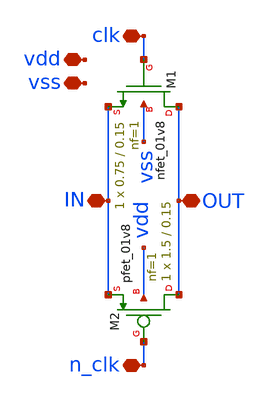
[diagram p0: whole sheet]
** sch_path: sch/TG.sch
**.subckt TG OUT IN clk n_clk vdd vss
*.iopin OUT
*.iopin IN
*.iopin clk
*.iopin n_clk
*.iopin vdd
*.iopin vss
XM1 OUT clk IN vss sky130_fd_pr__nfet_01v8 L=0.15 W=0.75 nf=1 ad='int((nf+1)/2) * W/nf * 0.29' as='int((nf+2)/2) * W/nf * 0.29'
+ pd='2*int((nf+1)/2) * (W/nf + 0.29)' ps='2*int((nf+2)/2) * (W/nf + 0.29)' nrd='0.29 / W' nrs='0.29 / W'
+ sa=0 sb=0 sd=0 mult=1 m=1
XM2 OUT n_clk IN vdd sky130_fd_pr__pfet_01v8 L=0.15 W=1.5 nf=1 ad='int((nf+1)/2) * W/nf * 0.29' as='int((nf+2)/2) * W/nf * 0.29'
+ pd='2*int((nf+1)/2) * (W/nf + 0.29)' ps='2*int((nf+2)/2) * (W/nf + 0.29)' nrd='0.29 / W' nrs='0.29 / W'
+ sa=0 sb=0 sd=0 mult=1 m=1
**.ends
.end
